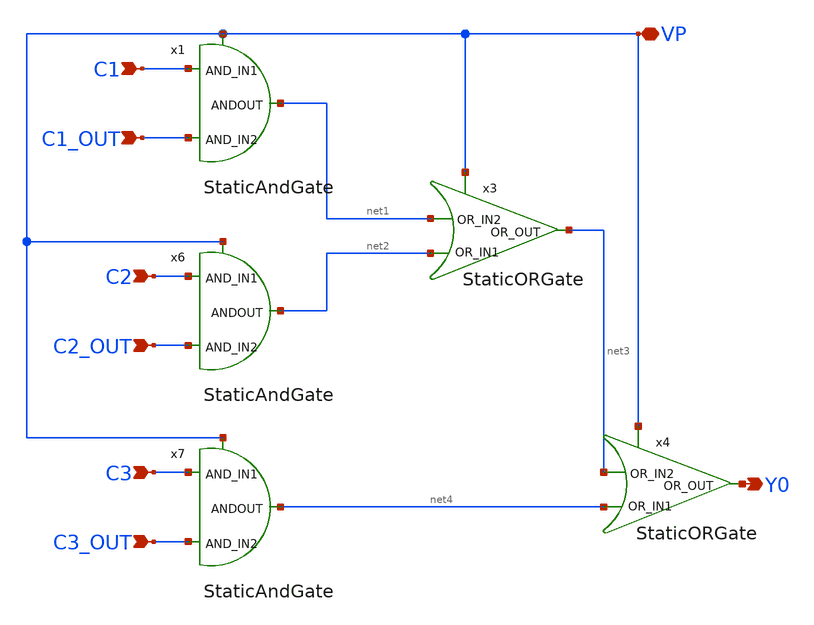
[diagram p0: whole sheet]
** sch_path: ALU_TOP_MODEL/OutputPortSel.sch
**.subckt OutputPortSel C1 C1_OUT C2 C2_OUT C3 C3_OUT VP Y0
*.ipin C1
*.ipin C1_OUT
*.ipin C2
*.ipin C2_OUT
*.ipin C3
*.ipin C3_OUT
*.iopin VP
*.opin Y0
x1 net1 C1 C1_OUT VP StaticAndGate
x6 net2 C2 C2_OUT VP StaticAndGate
x7 net4 C3 C3_OUT VP StaticAndGate
x3 net1 net2 net3 VP StaticORGate
x4 net3 net4 Y0 VP StaticORGate
**.ends

* expanding   symbol:
*+  /home/safal/projects/GitHub_CMOS_4bit_ALU/AllSymbols&Sch/Gates/StaticAndGate.sym # of pins=4
** sym_path: AllSymbols&Sch/Gates/StaticAndGate.sym
** sch_path: AllSymbols&Sch/Gates/StaticAndGate.sch
.subckt StaticAndGate ANDOUT AND_IN1 AND_IN2 VP
*.ipin AND_IN1
*.opin ANDOUT
*.ipin AND_IN2
*.iopin VP
XM1 net2 AND_IN2 VP VP sky130_fd_pr__pfet_01v8 L=0.15 W=1 nf=1 ad='int((1 + 1)/2) * 1 / 1 * 0.29' as='int((1 + 2)/2) * 1 / 1 * 0.29'
+ pd='2*int((1 + 1)/2) * (1 / 1 + 0.29)' ps='2*int((1 + 2)/2) * (1 / 1 + 0.29)' nrd='0.29 / 1 ' nrs='0.29 / 1 '
+ sa=0 sb=0 sd=0 mult=1 m=1
XM2 net2 AND_IN1 net1 net1 sky130_fd_pr__nfet_01v8 L=0.15 W=2 nf=1 ad='int((1 + 1)/2) * 2 / 1 * 0.29'
+ as='int((1 + 2)/2) * 2 / 1 * 0.29' pd='2*int((1 + 1)/2) * (2 / 1 + 0.29)' ps='2*int((1 + 2)/2) * (2 / 1 + 0.29)'
+ nrd='0.29 / 2 ' nrs='0.29 / 2 ' sa=0 sb=0 sd=0 mult=1 m=1
XM3 net1 AND_IN2 GND GND sky130_fd_pr__nfet_01v8 L=0.15 W=2 nf=1 ad='int((1 + 1)/2) * 2 / 1 * 0.29' as='int((1 + 2)/2) * 2 / 1 * 0.29'
+ pd='2*int((1 + 1)/2) * (2 / 1 + 0.29)' ps='2*int((1 + 2)/2) * (2 / 1 + 0.29)' nrd='0.29 / 2 ' nrs='0.29 / 2 '
+ sa=0 sb=0 sd=0 mult=1 m=1
XM4 net2 AND_IN1 VP VP sky130_fd_pr__pfet_01v8 L=0.15 W=1 nf=1 ad='int((1 + 1)/2) * 1 / 1 * 0.29' as='int((1 + 2)/2) * 1 / 1 * 0.29'
+ pd='2*int((1 + 1)/2) * (1 / 1 + 0.29)' ps='2*int((1 + 2)/2) * (1 / 1 + 0.29)' nrd='0.29 / 1 ' nrs='0.29 / 1 '
+ sa=0 sb=0 sd=0 mult=1 m=1
x1 VP ANDOUT net2 inverter
.ends


* expanding   symbol:
*+  /home/safal/projects/GitHub_CMOS_4bit_ALU/AllSymbols&Sch/Gates/StaticORGate.sym # of pins=4
** sym_path: AllSymbols&Sch/Gates/StaticORGate.sym
** sch_path: AllSymbols&Sch/Gates/StaticORGate.sch
.subckt StaticORGate OR_IN2 OR_IN1 OR_OUT VP
*.ipin OR_IN1
*.opin OR_OUT
*.ipin OR_IN2
*.iopin VP
XM1 net2 OR_IN1 net1 net1 sky130_fd_pr__pfet_01v8 L=0.15 W=8 nf=1 ad='int((1 + 1)/2) * 8 / 1 * 0.29'
+ as='int((1 + 2)/2) * 8 / 1 * 0.29' pd='2*int((1 + 1)/2) * (8 / 1 + 0.29)' ps='2*int((1 + 2)/2) * (8 / 1 + 0.29)'
+ nrd='0.29 / 8 ' nrs='0.29 / 8 ' sa=0 sb=0 sd=0 mult=1 m=1
XM2 net2 OR_IN1 GND GND sky130_fd_pr__nfet_01v8 L=0.15 W=1 nf=1 ad='int((1 + 1)/2) * 1 / 1 * 0.29' as='int((1 + 2)/2) * 1 / 1 * 0.29'
+ pd='2*int((1 + 1)/2) * (1 / 1 + 0.29)' ps='2*int((1 + 2)/2) * (1 / 1 + 0.29)' nrd='0.29 / 1 ' nrs='0.29 / 1 '
+ sa=0 sb=0 sd=0 mult=1 m=1
XM5 net1 OR_IN2 VP VP sky130_fd_pr__pfet_01v8 L=0.15 W=8 nf=1 ad='int((1 + 1)/2) * 8 / 1 * 0.29' as='int((1 + 2)/2) * 8 / 1 * 0.29'
+ pd='2*int((1 + 1)/2) * (8 / 1 + 0.29)' ps='2*int((1 + 2)/2) * (8 / 1 + 0.29)' nrd='0.29 / 8 ' nrs='0.29 / 8 '
+ sa=0 sb=0 sd=0 mult=1 m=1
XM6 net2 OR_IN2 GND GND sky130_fd_pr__nfet_01v8 L=0.15 W=1 nf=1 ad='int((1 + 1)/2) * 1 / 1 * 0.29' as='int((1 + 2)/2) * 1 / 1 * 0.29'
+ pd='2*int((1 + 1)/2) * (1 / 1 + 0.29)' ps='2*int((1 + 2)/2) * (1 / 1 + 0.29)' nrd='0.29 / 1 ' nrs='0.29 / 1 '
+ sa=0 sb=0 sd=0 mult=1 m=1
x1 VP OR_OUT net2 inverter
.ends


* expanding   symbol:
*+  /home/safal/projects/GitHub_CMOS_4bit_ALU/AllSymbols&Sch/GenericSym/inverter.sym # of pins=3
** sym_path: AllSymbols&Sch/GenericSym/inverter.sym
** sch_path: AllSymbols&Sch/GenericSym/inverter.sch
.subckt inverter VP inv_out inv_in
*.ipin inv_in
*.opin inv_out
*.iopin VP
XM1 inv_out inv_in VP VP sky130_fd_pr__pfet_01v8 L=0.15 W=2 nf=1 ad='int((1 + 1)/2) * 2 / 1 * 0.29' as='int((1 + 2)/2) * 2 / 1 * 0.29'
+ pd='2*int((1 + 1)/2) * (2 / 1 + 0.29)' ps='2*int((1 + 2)/2) * (2 / 1 + 0.29)' nrd='0.29 / 2 ' nrs='0.29 / 2 '
+ sa=0 sb=0 sd=0 mult=1 m=1
XM2 inv_out inv_in GND GND sky130_fd_pr__nfet_01v8 L=0.15 W=1 nf=1 ad='int((1 + 1)/2) * 1 / 1 * 0.29'
+ as='int((1 + 2)/2) * 1 / 1 * 0.29' pd='2*int((1 + 1)/2) * (1 / 1 + 0.29)' ps='2*int((1 + 2)/2) * (1 / 1 + 0.29)'
+ nrd='0.29 / 1 ' nrs='0.29 / 1 ' sa=0 sb=0 sd=0 mult=1 m=1
.ends

.GLOBAL GND
.end
